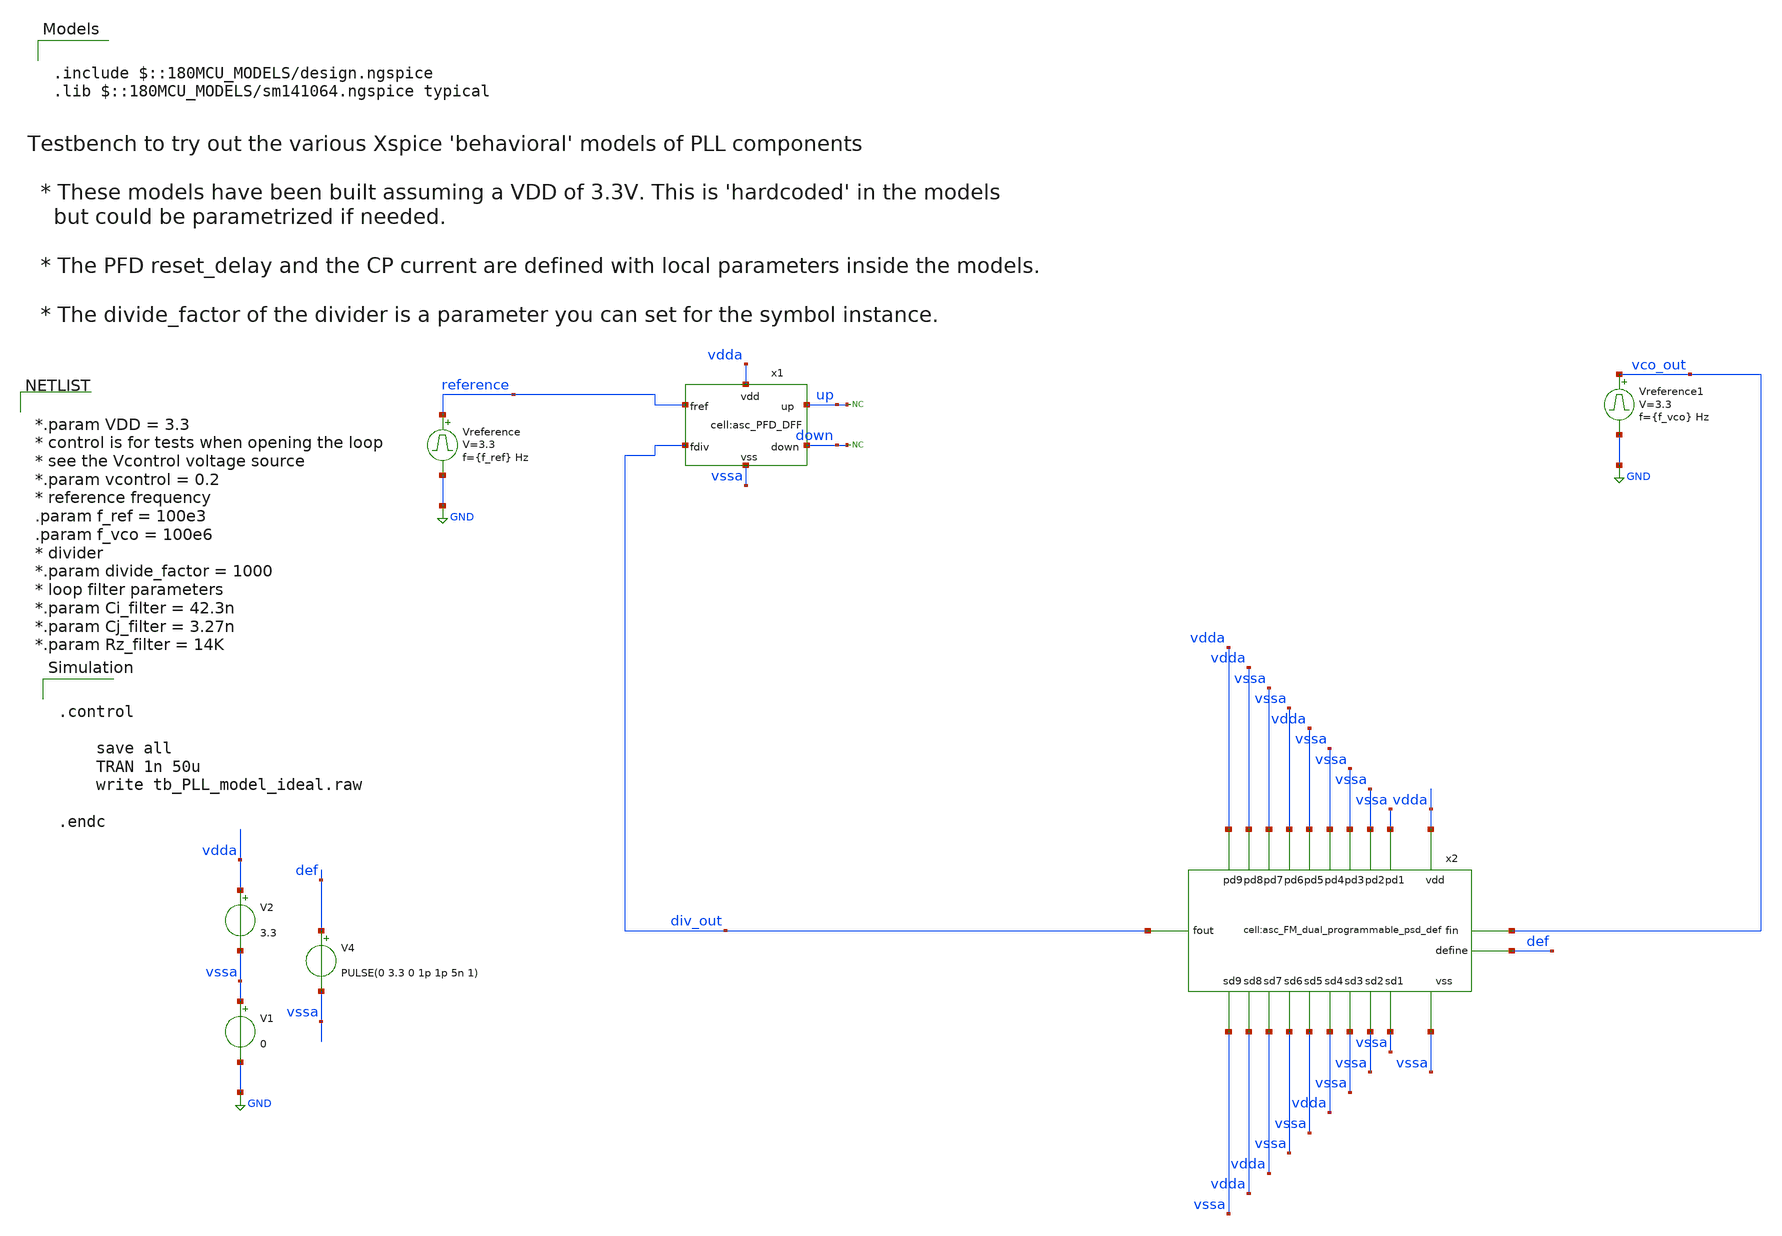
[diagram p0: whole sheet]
** sch_path: designs/libs/tb_analog/tb_single_pulse_psd/tb_single_pulse_psd.sch
**.subckt tb_single_pulse_psd
Vreference reference GND pulse 0 3.3 '0.495/ {f_ref} ' '0.01/{f_ref} ' '0.01/{f_ref} ' '0.49/{f_ref} '
+ '1/{f_ref} '
V1 vssa GND 0
V2 vdda vssa 3.3
V4 def vssa PULSE(0 3.3 0 1p 1p 5n 1)
x1 vdda vssa down up reference div_out asc_PFD_DFF
* noconn up
* noconn down
Vreference1 vco_out GND pulse 0 3.3 '0.495/ {f_vco} ' '0.01/{f_vco} ' '0.01/{f_vco} ' '0.49/{f_vco} '
+ '1/{f_vco} '
**** begin user architecture code


.control

    save all
    TRAN 1n 50u
    write tb_PLL_model_ideal.raw

.endc




*.param VDD = 3.3
* control is for tests when opening the loop
* see the Vcontrol voltage source
*.param vcontrol = 0.2
* reference frequency
.param f_ref = 100e3
.param f_vco = 100e6
* divider
*.param divide_factor = 1000
* loop filter parameters
*.param Ci_filter = 42.3n
*.param Cj_filter = 3.27n
*.param Rz_filter = 14K



.include $::180MCU_MODELS/design.ngspice
.lib $::180MCU_MODELS/sm141064.ngspice typical

**** end user architecture code
**.ends
.GLOBAL GND
.end
